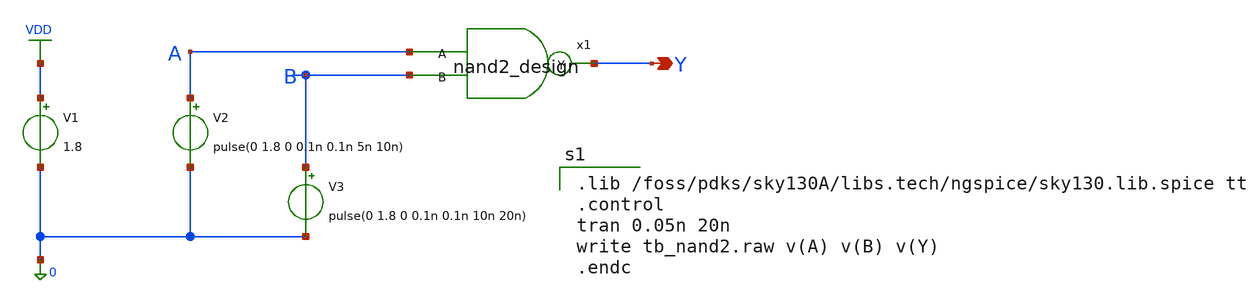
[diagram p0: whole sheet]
** sch_path: cells/full_adder_tg/xschem/tb_nand2_part.sch
**.subckt tb_nand2_part Y
*.opin Y
V1 VDD 0 1.8
V2 A 0 pulse(0 1.8 0 0.1n 0.1n 5n 10n)
V3 B 0 pulse(0 1.8 0 0.1n 0.1n 10n 20n)
x1 A Y B nand2_design
**** begin user architecture code

.lib /foss/pdks/sky130A/libs.tech/ngspice/sky130.lib.spice tt
.control
tran 0.05n 20n
write tb_nand2.raw v(A) v(B) v(Y)
.endc

**** end user architecture code
**.ends

* expanding   symbol:  ./nand2_design.sym # of pins=3
** sym_path: cells/full_adder_tg/xschem/nand2_design.sym
** sch_path: cells/full_adder_tg/xschem/nand2_design.sch
.subckt nand2_design A Y B
*.ipin A
*.ipin B
*.opin Y
XPMOS_1 Y A VDD VDD sky130_fd_pr__pfet_01v8 L=0.15 W=6 nf=1 ad='int((1 + 1)/2) * 6 / 1 * 0.29' as='int((1 + 2)/2) * 6 / 1 * 0.29'
+ pd='2*int((1 + 1)/2) * (6 / 1 + 0.29)' ps='2*int((1 + 2)/2) * (6 / 1 + 0.29)' nrd='0.29 / 6 ' nrs='0.29 / 6 '
+ sa=0 sb=0 sd=0 mult=1 m=1
XPMOS_2 Y B VDD VDD sky130_fd_pr__pfet_01v8 L=0.15 W=6 nf=1 ad='int((1 + 1)/2) * 6 / 1 * 0.29' as='int((1 + 2)/2) * 6 / 1 * 0.29'
+ pd='2*int((1 + 1)/2) * (6 / 1 + 0.29)' ps='2*int((1 + 2)/2) * (6 / 1 + 0.29)' nrd='0.29 / 6 ' nrs='0.29 / 6 '
+ sa=0 sb=0 sd=0 mult=1 m=1
XNMOS_1 Y A net1 0 sky130_fd_pr__nfet_01v8 L=0.15 W=3 nf=1 ad='int((1 + 1)/2) * 3 / 1 * 0.29' as='int((1 + 2)/2) * 3 / 1 * 0.29'
+ pd='2*int((1 + 1)/2) * (3 / 1 + 0.29)' ps='2*int((1 + 2)/2) * (3 / 1 + 0.29)' nrd='0.29 / 3 ' nrs='0.29 / 3 '
+ sa=0 sb=0 sd=0 mult=1 m=1
XNMOS_2 net1 B 0 0 sky130_fd_pr__nfet_01v8 L=0.15 W=3 nf=1 ad='int((1 + 1)/2) * 3 / 1 * 0.29' as='int((1 + 2)/2) * 3 / 1 * 0.29'
+ pd='2*int((1 + 1)/2) * (3 / 1 + 0.29)' ps='2*int((1 + 2)/2) * (3 / 1 + 0.29)' nrd='0.29 / 3 ' nrs='0.29 / 3 '
+ sa=0 sb=0 sd=0 mult=1 m=1
.ends

.GLOBAL VDD
.end
